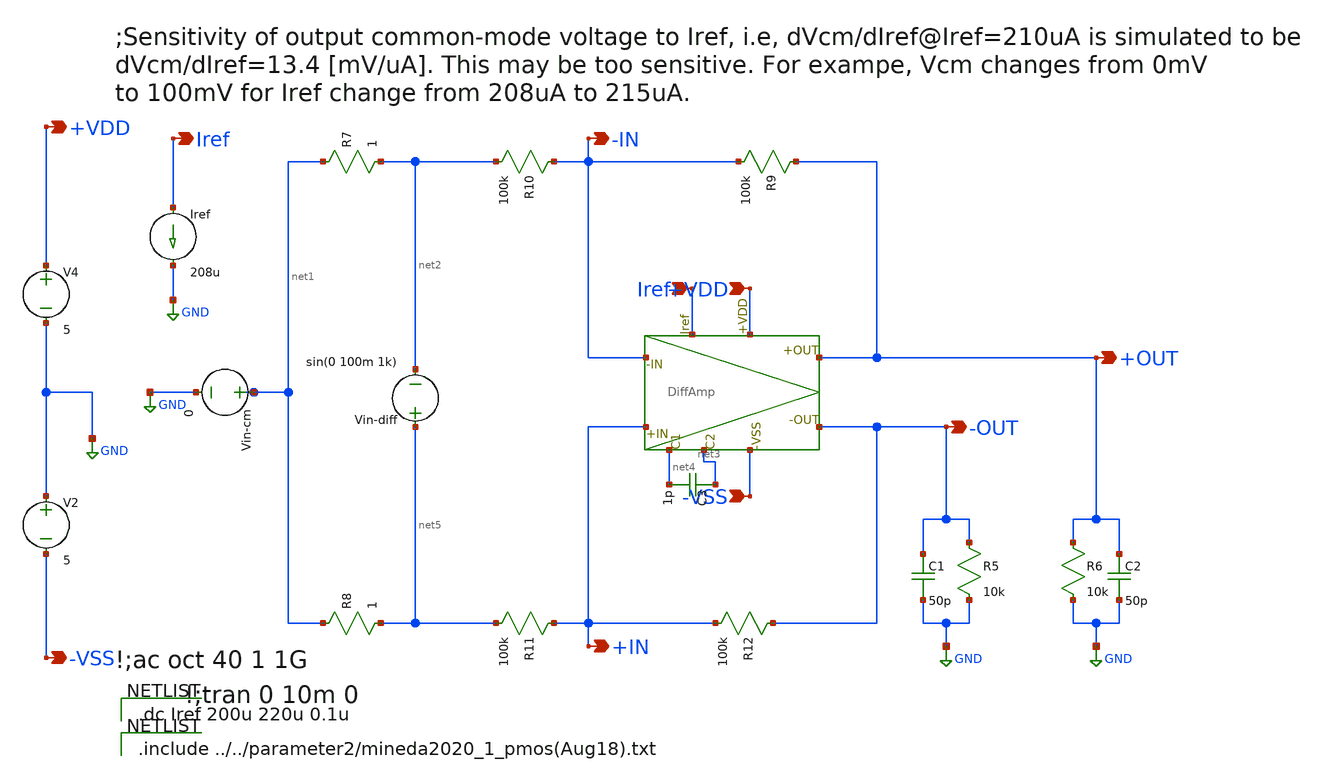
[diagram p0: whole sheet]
** sch_path: mmm-CMoutSensitivity.sch
**.subckt mmm-CMoutSensitivity +VDD -VSS Iref -OUT +OUT +IN -IN +VDD -VSS Iref
*.opin +VDD
*.opin -VSS
*.opin Iref
*.opin -OUT
*.opin +OUT
*.opin +IN
*.opin -IN
*.ipin +VDD
*.ipin -VSS
*.ipin Iref
Iref Iref GND 208u
Vin-diff net5 net2 sin(0 100m 1k)
V2 GND -VSS 5
R5 -OUT GND 10k m=1
R6 +OUT GND 10k m=1
V4 +VDD GND 5
R7 net1 net2 1 m=1
R8 net1 net5 1 m=1
C1 -OUT GND 50p m=1
C2 +OUT GND 50p m=1
Vin-cm net1 GND 0
R9 +OUT -IN 100k m=1
R10 -IN net2 100k m=1
R11 +IN net5 100k m=1
R12 -OUT +IN 100k m=1
C3 net3 net4 1p m=1
X1 +IN -IN -OUT +OUT +VDD -VSS net4 net3 Iref DiffAmp
**** begin user architecture code

.dc Iref 200u 220u 0.1u


.include ../../parameter2/mineda2020_1_pmos(Aug18).txt

**** end user architecture code
**.ends

* expanding   symbol:  DiffAmp.sym # of pins=9
** sym_path: DiffAmp.sym
** sch_path: DiffAmp.sch
.subckt DiffAmp +IN -IN -OUT +OUT +VDD -VSS C1 C2 Iref
*.opin -OUT
*.opin +OUT
*.ipin +VDD
*.ipin -VSS
*.ipin Iref
*.ipin +IN
*.ipin -IN
*.iopin C1
*.iopin C2
**** begin user architecture code

.include ../../parameter2/mineda2020_1_pmos(Aug18).txt

**** end user architecture code
**** begin user architecture code

.ac oct 40 1 1G

**** end user architecture code
M6 Iref net1 +VDD +VDD YSS_PMOS w=280u l=14u as=3.92n ps=308u ad=3.92n pd=308u m=1
M2 net7 Iref net1 +VDD YSS_PMOS w=84u l=14u as=1.176n ps=112u ad=1.176n pd=112u m=1
M3 net11 +IN net7 +VDD YSS_PMOS w=200u l=10u as=2.0n ps=220u ad=2.0n pd=220u m=1
R1 net11 -VSS 30k m=1
R2 net12 -VSS 30k m=1
R3 C1 -VSS 30k m=1
R4 C2 -VSS 30k m=1
M4 net1 net1 +VDD +VDD YSS_PMOS w=280u l=14u as=3.92n ps=308u ad=3.92n pd=308u m=1
M5 net4 net1 +VDD +VDD YSS_PMOS w=280u l=14u as=3.92n ps=308u ad=3.92n pd=308u m=1
M7 net8 Iref net4 +VDD YSS_PMOS w=84u l=14u as=1.176n ps=112u ad=1.176n pd=112u m=1
M8 C1 net10 net8 +VDD YSS_PMOS w=200u l=10u as=2.0n ps=220u ad=2.0n pd=220u m=1
M1 net12 -IN net7 +VDD YSS_PMOS w=200u l=10u as=2.0n ps=220u ad=2.0n pd=220u m=1
M9 C2 net9 net8 +VDD YSS_PMOS w=200u l=10u as=2.0n ps=220u ad=2.0n pd=220u m=1
M10 net2 net1 +VDD +VDD YSS_PMOS w=280u l=14u as=3.92n ps=308u ad=3.92n pd=308u m=1
M11 net10 Iref net2 +VDD YSS_PMOS w=84u l=14u as=1.176n ps=112u ad=1.176n pd=112u m=1
M12 -VSS net11 net10 +VDD YSS_PMOS w=200u l=10u as=2.0n ps=220u ad=2.0n pd=220u m=1
M13 -VSS net12 net9 +VDD YSS_PMOS w=200u l=10u as=2.0n ps=220u ad=2.0n pd=220u m=1
M14 net3 net1 +VDD +VDD YSS_PMOS w=280u l=14u as=3.92n ps=308u ad=3.92n pd=308u m=1
M15 net9 Iref net3 +VDD YSS_PMOS w=84u l=14u as=1.176n ps=112u ad=1.176n pd=112u m=1
M16 net5 net1 +VDD +VDD YSS_PMOS w=280u l=14u as=3.92n ps=308u ad=3.92n pd=308u m=4
M17 +OUT Iref net5 +VDD YSS_PMOS w=84u l=14u as=1.176n ps=112u ad=1.176n pd=112u m=4
M18 -VSS C1 +OUT +VDD YSS_PMOS w=200u l=10u as=2.0n ps=220u ad=2.0n pd=220u m=4
M19 -VSS C2 -OUT +VDD YSS_PMOS w=200u l=10u as=2.0n ps=220u ad=2.0n pd=220u m=4
M20 net6 net1 +VDD +VDD YSS_PMOS w=280u l=14u as=3.92n ps=308u ad=3.92n pd=308u m=4
M21 -OUT Iref net6 +VDD YSS_PMOS w=84u l=14u as=1.176n ps=112u ad=1.176n pd=112u m=4
C9 C2 C1 50p m=1
.ends

.GLOBAL GND
.end
